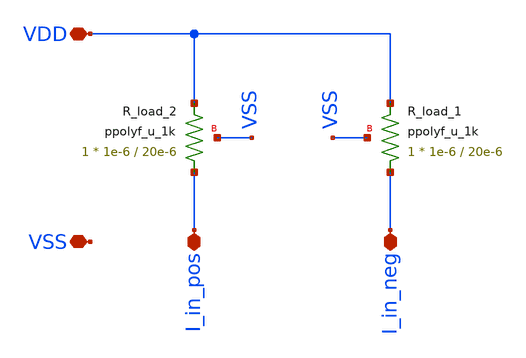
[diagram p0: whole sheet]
** sch_path: designs/libs/core_top/A5_Time_Transcenders/schematics/Gilbert_cell_hierarchal_loading_stage.sch
**.subckt Gilbert_cell_hierarchal_loading_stage I_in_neg I_in_pos VDD VSS
*.iopin I_in_neg
*.iopin I_in_pos
*.iopin VDD
*.iopin VSS
XR_load_2 I_in_pos VDD VSS ppolyf_u_1k r_width=1e-6 r_length=20e-6 m=1
XR_load_1 I_in_neg VDD VSS ppolyf_u_1k r_width=1e-6 r_length=20e-6 m=1
**.ends
.end
